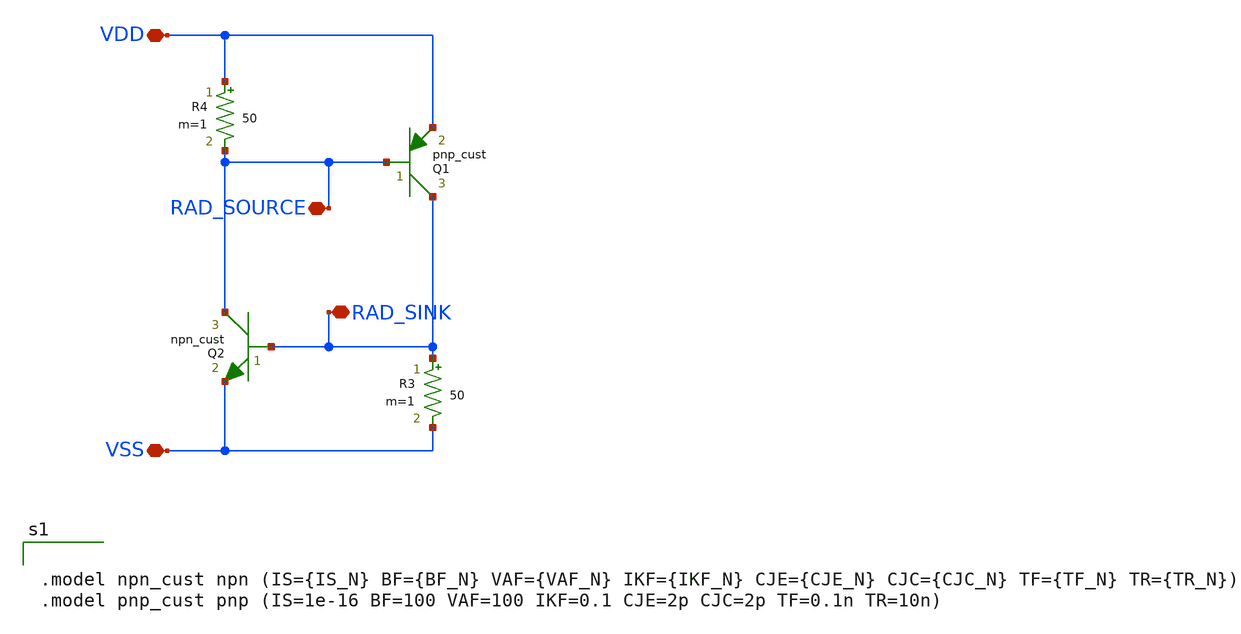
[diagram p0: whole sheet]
** sch_path: latchup/basic_model.sch
**.subckt basic_model VDD VSS RAD_SOURCE RAD_SINK
*.iopin VDD
*.iopin VSS
*.iopin RAD_SOURCE
*.iopin RAD_SINK
Q1 RAD_SINK RAD_SOURCE VDD pnp_cust area=1 m=1
Q2 RAD_SOURCE RAD_SINK VSS npn_cust area=1 m=1
R3 RAD_SINK VSS 50 m=1
R4 VDD RAD_SOURCE 50 m=1
**** begin user architecture code


.model npn_cust npn (IS={IS_N} BF={BF_N} VAF={VAF_N} IKF={IKF_N} CJE={CJE_N} CJC={CJC_N} TF={TF_N} TR={TR_N})
.model pnp_cust pnp (IS=1e-16 BF=100 VAF=100 IKF=0.1 CJE=2p CJC=2p TF=0.1n TR=10n)


**** end user architecture code
**.ends
.end
